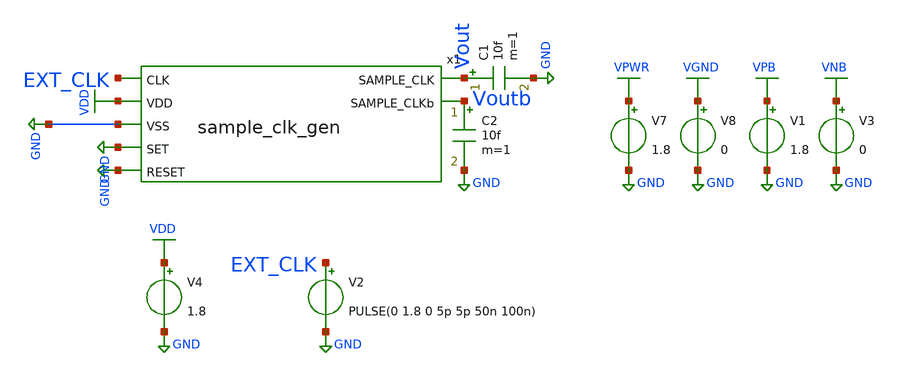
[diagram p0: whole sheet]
** sch_path: module/sample_clk_gen_default_device/tb_sample_clk_gen.sch
**.subckt tb_sample_clk_gen
V2 EXT_CLK GND PULSE(0 1.8 0 5p 5p 50n 100n)
V4 VDD GND 1.8
x1 Vout Voutb EXT_CLK VDD GND GND GND sample_clk_gen
C1 Vout GND 10f m=1
V1 VPB GND 1.8
V3 VNB GND 0
V7 VPWR GND 1.8
V8 VGND GND 0
C2 Voutb GND 10f m=1
**** begin user architecture code



.lib /foss/pdks/sky130A/libs.tech/ngspice/sky130.lib.spice tt
.include /foss/pdks/sky130A/libs.ref/sky130_fd_sc_hd/spice/sky130_fd_sc_hd.spice

.tran 1ps 200ns

.control
	run
	plot V(Vout) V(Voutb) V(EXT_CLK)
.endc
.save all



**** end user architecture code
**.ends
.GLOBAL GND
.GLOBAL VDD
.GLOBAL VPB
.GLOBAL VNB
.GLOBAL VPWR
.GLOBAL VGND
.end
